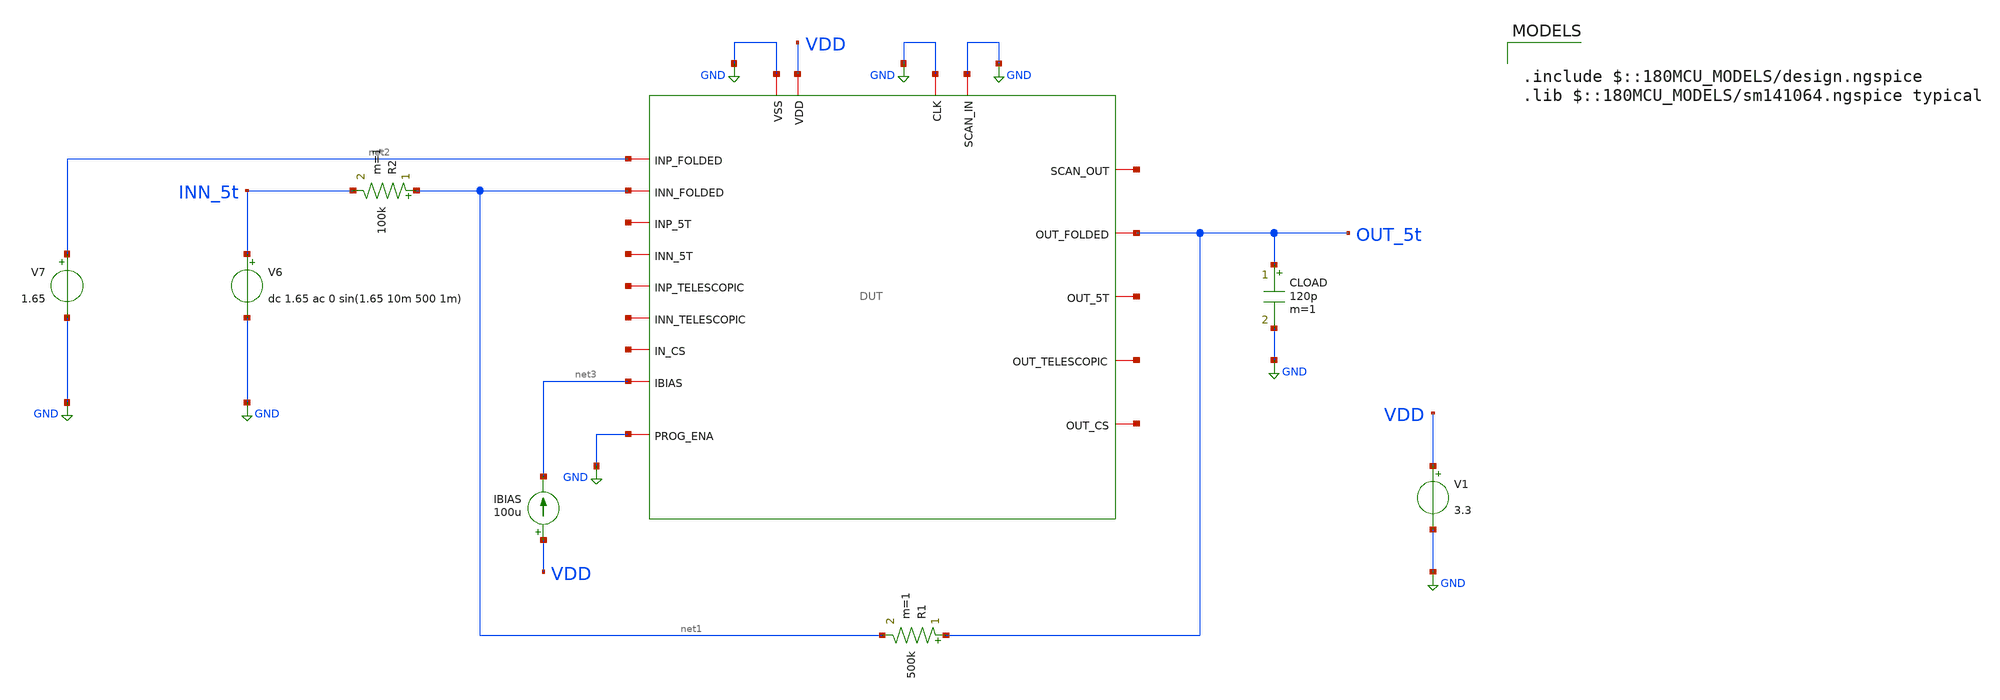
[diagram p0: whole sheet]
** sch_path: designs/libs/core_tb/sl/PEX_start_up_no_cap/default_inverting_5t.sch
**.subckt default_inverting_5t
V1 VDD GND 3.3
CLOAD OUT_5t GND 120p m=1
R1 OUT_5t net1 500k m=1
R2 net1 INN_5t 100k m=1
V6 INN_5t GND dc 1.65 ac 0 sin(1.65 10m 500 1m)
V7 net2 GND 1.65
IBIAS VDD net3 100u
x1 GND net4 GND GND VDD OUT_5t net2 net5 net3 net1 net6 net7 net8 net9 net10 net11 net12 GND DUT
**** begin user architecture code

.include $::180MCU_MODELS/design.ngspice
.lib $::180MCU_MODELS/sm141064.ngspice typical



.include /foss/designs/libs/pex/DUT.spice
.control
tran 1u 5m

set color0 = white
set color1 = black

plot v(out_5t) v(inn_5t)
wrdata /foss/designs/libs/core_tb/sl/PEX_start_up_no_cap/default.csv v(out_5T) v(inn_5T)

meas tran vout_pp pp v(out_5t) from=2m to=5m
meas tran vin_pp pp v(inn_5t) from=2m to=5m
let gain = vout_pp / vin_pp
print gain

meas tran vout_dc avg v(out_5t) from=2m to=5m
meas tran vin_dc avg v(inn_5t) from=2m to=5m
let dc_offset = vout_dc - vin_dc
let input_offset = dc_offset / 6
print vout_dc vin_dc dc_offset input_offset

let ideal_gain = 5
let gain_error_pct = (ideal_gain - gain) / ideal_gain * 100
print gain_error_pct

meas tran idd avg i(v1) from=2m to=5m
let power = abs(idd) * 3.3
print idd power

.endc


**** end user architecture code
**.ends
.GLOBAL GND
.end
